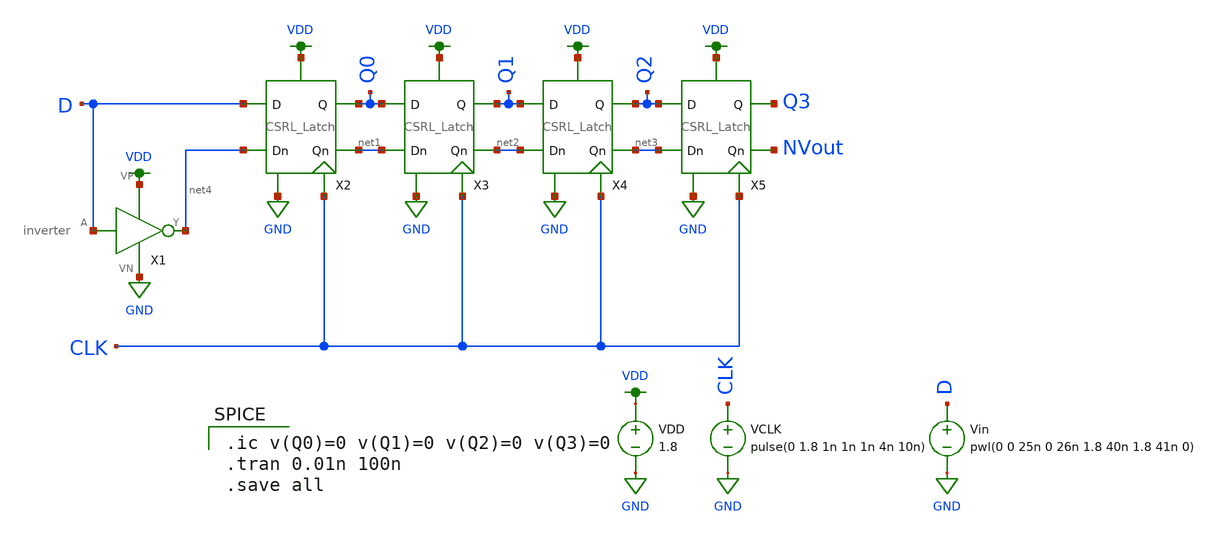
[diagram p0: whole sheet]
** sch_path: shift register/CSRL_Latch_simulation.sch
**.subckt CSRL_Latch_simulation
VDD VDD GND 1.8
VCLK CLK GND pulse(0 1.8 1n 1n 1n 4n 10n)
Vin D GND pwl(0 0 25n 0 26n 1.8 40n 1.8 41n 0)
X1 D net4 VDD GND inverter
X2 D Q0 VDD GND CLK net4 net1 CSRL_Latch
X3 Q0 Q1 VDD GND CLK net1 net2 CSRL_Latch
X4 Q1 Q2 VDD GND CLK net2 net3 CSRL_Latch
X5 Q2 Q3 VDD GND CLK net3 NVout CSRL_Latch
**** begin user architecture code

.ic v(Q0)=0 v(Q1)=0 v(Q2)=0 v(Q3)=0
.tran 0.01n 100n
.save all


.option wnflag=1
.lib ~/skywater/skywater-pdk/libraries/sky130_fd_pr_ngspice/latest/models/sky130.lib.spice sf

**** end user architecture code
**.ends
.GLOBAL VDD
.GLOBAL GND
.end
